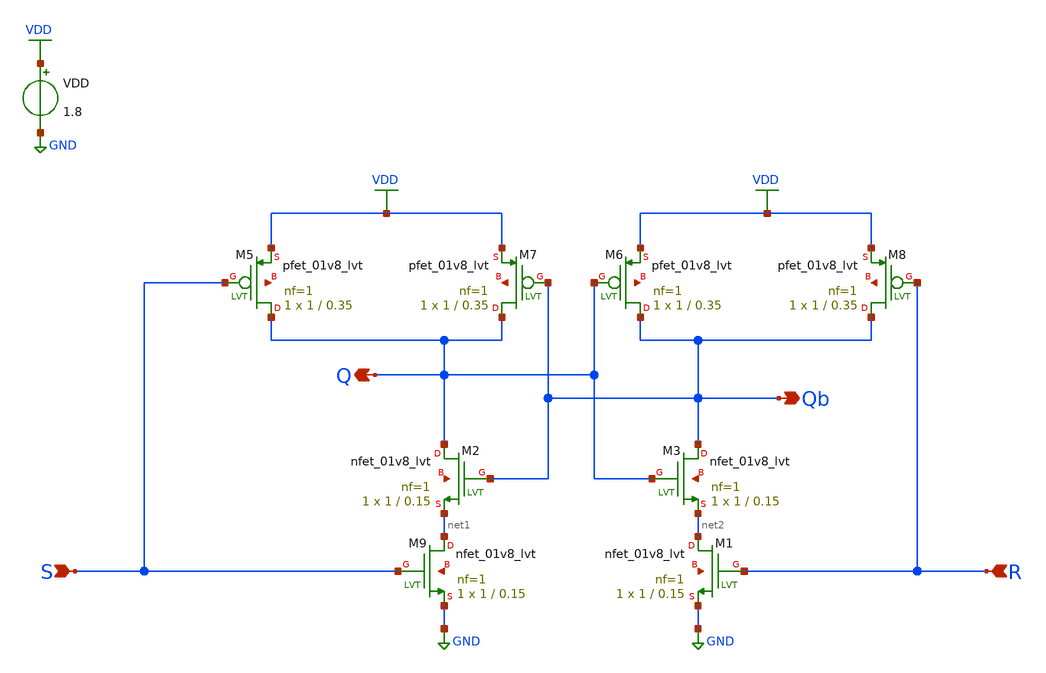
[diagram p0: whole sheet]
** sch_path: ZCD/sr_latch.sch
**.subckt sr_latch S R Qb Q
*.ipin S
*.ipin R
*.opin Qb
*.opin Q
XM9 net1 S GND net3 sky130_fd_pr__nfet_01v8_lvt L=0.15 W=1 nf=1 ad='int((nf+1)/2) * W/nf * 0.29' as='int((nf+2)/2) * W/nf * 0.29'
+ pd='2*int((nf+1)/2) * (W/nf + 0.29)' ps='2*int((nf+2)/2) * (W/nf + 0.29)' nrd='0.29 / W' nrs='0.29 / W'
+ sa=0 sb=0 sd=0 mult=1 m=1
XM1 net2 R GND net4 sky130_fd_pr__nfet_01v8_lvt L=0.15 W=1 nf=1 ad='int((nf+1)/2) * W/nf * 0.29' as='int((nf+2)/2) * W/nf * 0.29'
+ pd='2*int((nf+1)/2) * (W/nf + 0.29)' ps='2*int((nf+2)/2) * (W/nf + 0.29)' nrd='0.29 / W' nrs='0.29 / W'
+ sa=0 sb=0 sd=0 mult=1 m=1
XM2 Q Qb net1 net5 sky130_fd_pr__nfet_01v8_lvt L=0.15 W=1 nf=1 ad='int((nf+1)/2) * W/nf * 0.29' as='int((nf+2)/2) * W/nf * 0.29'
+ pd='2*int((nf+1)/2) * (W/nf + 0.29)' ps='2*int((nf+2)/2) * (W/nf + 0.29)' nrd='0.29 / W' nrs='0.29 / W'
+ sa=0 sb=0 sd=0 mult=1 m=1
XM3 Qb Q net2 net6 sky130_fd_pr__nfet_01v8_lvt L=0.15 W=1 nf=1 ad='int((nf+1)/2) * W/nf * 0.29' as='int((nf+2)/2) * W/nf * 0.29'
+ pd='2*int((nf+1)/2) * (W/nf + 0.29)' ps='2*int((nf+2)/2) * (W/nf + 0.29)' nrd='0.29 / W' nrs='0.29 / W'
+ sa=0 sb=0 sd=0 mult=1 m=1
XM5 Q S VDD net7 sky130_fd_pr__pfet_01v8_lvt L=0.35 W=1 nf=1 ad='int((nf+1)/2) * W/nf * 0.29' as='int((nf+2)/2) * W/nf * 0.29'
+ pd='2*int((nf+1)/2) * (W/nf + 0.29)' ps='2*int((nf+2)/2) * (W/nf + 0.29)' nrd='0.29 / W' nrs='0.29 / W'
+ sa=0 sb=0 sd=0 mult=1 m=1
XM6 Qb Q VDD net8 sky130_fd_pr__pfet_01v8_lvt L=0.35 W=1 nf=1 ad='int((nf+1)/2) * W/nf * 0.29' as='int((nf+2)/2) * W/nf * 0.29'
+ pd='2*int((nf+1)/2) * (W/nf + 0.29)' ps='2*int((nf+2)/2) * (W/nf + 0.29)' nrd='0.29 / W' nrs='0.29 / W'
+ sa=0 sb=0 sd=0 mult=1 m=1
XM7 Q Qb VDD net9 sky130_fd_pr__pfet_01v8_lvt L=0.35 W=1 nf=1 ad='int((nf+1)/2) * W/nf * 0.29' as='int((nf+2)/2) * W/nf * 0.29'
+ pd='2*int((nf+1)/2) * (W/nf + 0.29)' ps='2*int((nf+2)/2) * (W/nf + 0.29)' nrd='0.29 / W' nrs='0.29 / W'
+ sa=0 sb=0 sd=0 mult=1 m=1
XM8 Qb R VDD net10 sky130_fd_pr__pfet_01v8_lvt L=0.35 W=1 nf=1 ad='int((nf+1)/2) * W/nf * 0.29' as='int((nf+2)/2) * W/nf * 0.29'
+ pd='2*int((nf+1)/2) * (W/nf + 0.29)' ps='2*int((nf+2)/2) * (W/nf + 0.29)' nrd='0.29 / W' nrs='0.29 / W'
+ sa=0 sb=0 sd=0 mult=1 m=1
VDD VDD GND 1.8
**.ends
.GLOBAL VDD
.GLOBAL GND
.end
